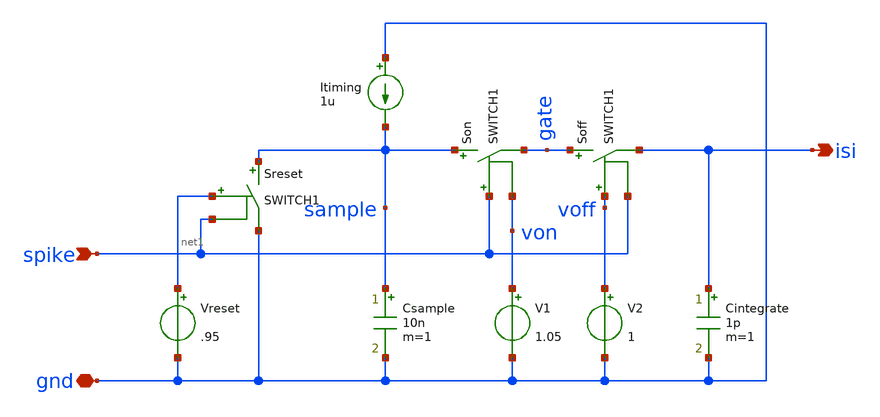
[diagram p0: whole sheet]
** sch_path: playground/InterServicesIntelligence.sch
**.subckt InterServicesIntelligence gnd spike isi
*.iopin gnd
*.ipin spike
*.opin isi
Csample sample gnd 10n m=1
Itiming gnd sample 1u
Son sample gate spike von SWITCH1
Sreset sample gnd net1 spike SWITCH1
Cintegrate isi gnd 1p m=1
V1 von gnd 1.05
Vreset net1 gnd .95
Soff gate isi voff spike SWITCH1
V2 voff gnd 1
**.ends
.end
